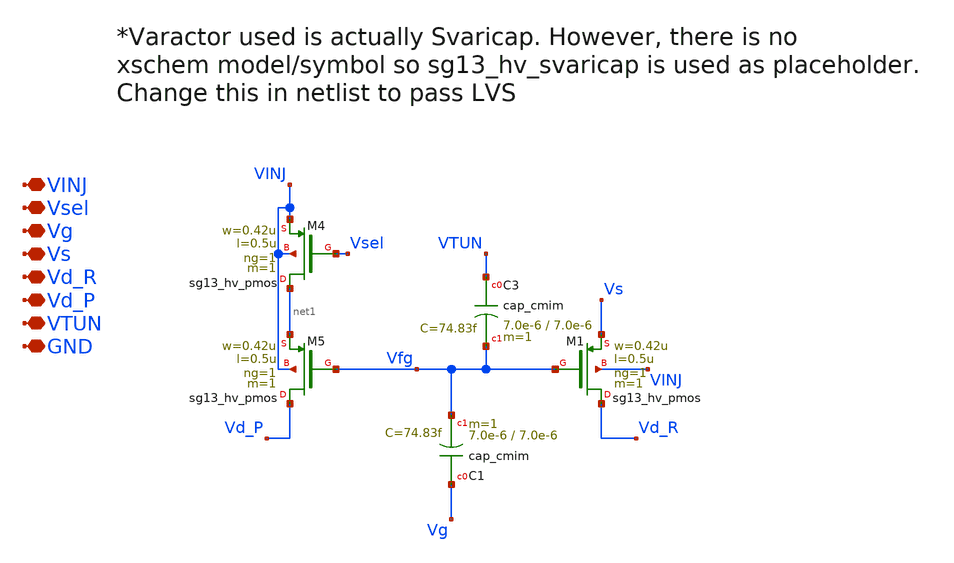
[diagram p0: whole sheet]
** sch_path: ihp130_cells/FG_Indirect/FG_Indirect.sch
**.subckt FG_Indirect VINJ Vsel Vg Vs Vd_R Vd_P VTUN GND
*.iopin VINJ
*.iopin Vsel
*.iopin Vg
*.iopin Vs
*.iopin Vd_R
*.iopin Vd_P
*.iopin VTUN
*.iopin GND
XM4 net1 Vsel VINJ VINJ sg13_hv_pmos w=0.42u l=0.5u ng=1 m=1 mm_ok=1
XM5 Vd_P Vfg net1 VINJ sg13_hv_pmos w=0.42u l=0.5u ng=1 m=1 mm_ok=1
XM1 Vd_R Vfg Vs VINJ sg13_hv_pmos w=0.42u l=0.5u ng=1 m=1 mm_ok=1
XC3 VTUN Vfg cap_cmim w=7.0e-6 l=7.0e-6 m=1 mm_ok=1
XC1 Vg Vfg cap_cmim w=7.0e-6 l=7.0e-6 m=1 mm_ok=1
**.ends
.end
